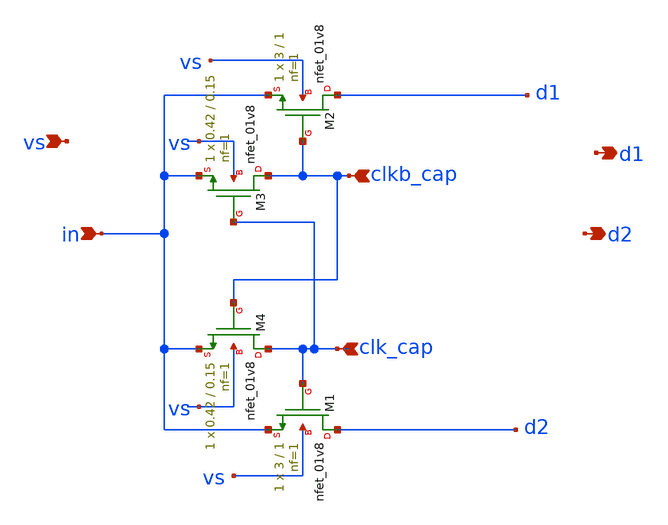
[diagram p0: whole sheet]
** sch_path: xschem/charge_pumps2/nmos_dnw_cp2.sch
**.subckt nmos_dnw_cp2 in d1 d2 vs clkb_cap clk_cap
*.ipin in
*.opin d1
*.opin d2
*.ipin vs
*.ipin clkb_cap
*.ipin clk_cap
XM2 d1 clkb_cap in vs sky130_fd_pr__nfet_01v8 L=1 W=3 nf=1 ad='int((nf+1)/2) * W/nf * 0.29' as='int((nf+2)/2) * W/nf * 0.29'
+ pd='2*int((nf+1)/2) * (W/nf + 0.29)' ps='2*int((nf+2)/2) * (W/nf + 0.29)' nrd='0.29 / W' nrs='0.29 / W'
+ sa=0 sb=0 sd=0 mult=1 m=1
XM1 d2 clk_cap in vs sky130_fd_pr__nfet_01v8 L=1 W=3 nf=1 ad='int((nf+1)/2) * W/nf * 0.29' as='int((nf+2)/2) * W/nf * 0.29'
+ pd='2*int((nf+1)/2) * (W/nf + 0.29)' ps='2*int((nf+2)/2) * (W/nf + 0.29)' nrd='0.29 / W' nrs='0.29 / W'
+ sa=0 sb=0 sd=0 mult=1 m=1
XM3 clkb_cap clk_cap in vs sky130_fd_pr__nfet_01v8 L=0.15 W=0.42 nf=1 ad='int((nf+1)/2) * W/nf * 0.29'
+ as='int((nf+2)/2) * W/nf * 0.29' pd='2*int((nf+1)/2) * (W/nf + 0.29)' ps='2*int((nf+2)/2) * (W/nf + 0.29)'
+ nrd='0.29 / W' nrs='0.29 / W' sa=0 sb=0 sd=0 mult=1 m=1
XM4 clk_cap clkb_cap in vs sky130_fd_pr__nfet_01v8 L=0.15 W=0.42 nf=1 ad='int((nf+1)/2) * W/nf * 0.29'
+ as='int((nf+2)/2) * W/nf * 0.29' pd='2*int((nf+1)/2) * (W/nf + 0.29)' ps='2*int((nf+2)/2) * (W/nf + 0.29)'
+ nrd='0.29 / W' nrs='0.29 / W' sa=0 sb=0 sd=0 mult=1 m=1
**.ends
.end
